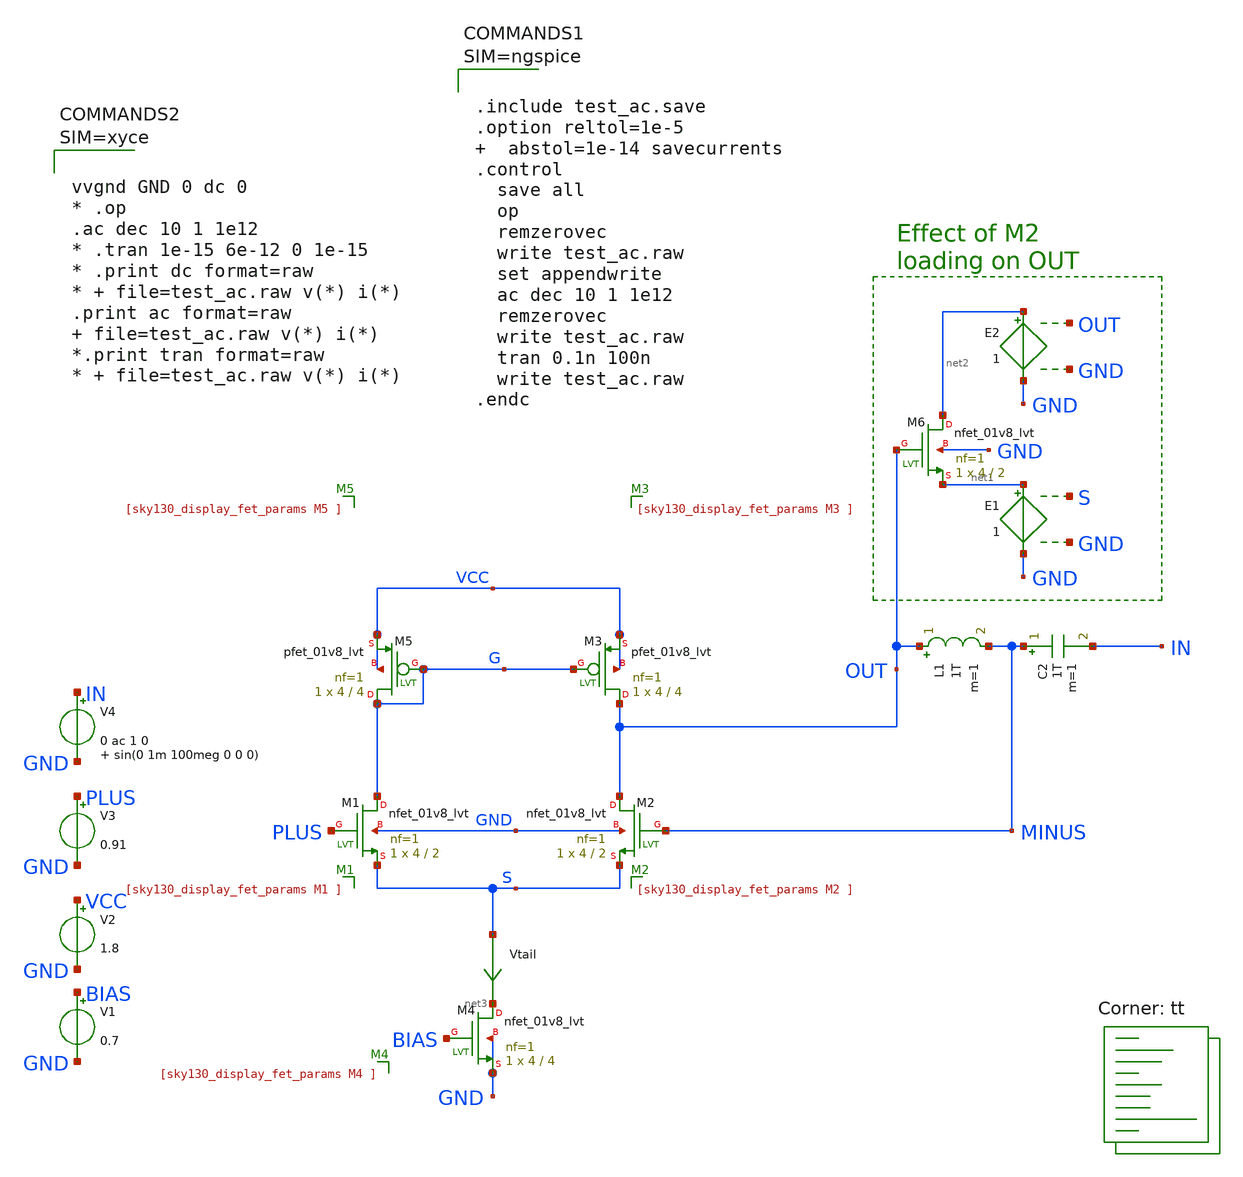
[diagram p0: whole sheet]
** sch_path: sky130A/xschem_libs/sky130_tests/test_ac/schematic/test_ac.sch
* Copyright 2021 Stefan Frederik Schippers
* Licensed under the Apache License, Version 2.0 (the "License");
* you may not use this file except in compliance with the License.
* You may obtain a copy of the License at
* https://www.apache.org/licenses/LICENSE-2.0
* Unless required by applicable law or agreed to in writing, software
* distributed under the License is distributed on an "AS IS" BASIS,
* WITHOUT WARRANTIES OR CONDITIONS OF ANY KIND, either express or implied.
* See the License for the specific language governing permissions and
* limitations under the License.
**.subckt test_ac
XM1 G PLUS S GND sky130_fd_pr__nfet_01v8_lvt L=2 W=4 nf=1 ad='int((1 + 1)/2) * 4 / 1 * 0.29' as='int((1 + 2)/2) * 4 / 1 * 0.29'
+ pd='2*int((1 + 1)/2) * (4 / 1 + 0.29)' ps='2*int((1 + 2)/2) * (4 / 1 + 0.29)' nrd='0.29 / 4 ' nrs='0.29 / 4 '
+ sa=0 sb=0 sd=0 mult=1 m=1
XM2 OUT MINUS S GND sky130_fd_pr__nfet_01v8_lvt L=2 W=4 nf=1 ad='int((1 + 1)/2) * 4 / 1 * 0.29' as='int((1 + 2)/2) * 4 / 1 * 0.29'
+ pd='2*int((1 + 1)/2) * (4 / 1 + 0.29)' ps='2*int((1 + 2)/2) * (4 / 1 + 0.29)' nrd='0.29 / 4 ' nrs='0.29 / 4 '
+ sa=0 sb=0 sd=0 mult=1 m=1
XM4 net3 BIAS GND GND sky130_fd_pr__nfet_01v8_lvt L=4 W=4 nf=1 ad='int((1 + 1)/2) * 4 / 1 * 0.29' as='int((1 + 2)/2) * 4 / 1 * 0.29'
+ pd='2*int((1 + 1)/2) * (4 / 1 + 0.29)' ps='2*int((1 + 2)/2) * (4 / 1 + 0.29)' nrd='0.29 / 4 ' nrs='0.29 / 4 '
+ sa=0 sb=0 sd=0 mult=1 m=1
XM3 OUT G VCC VCC sky130_fd_pr__pfet_01v8_lvt L=4 W=4 nf=1 ad='int((1 + 1)/2) * 4 / 1 * 0.29' as='int((1 + 2)/2) * 4 / 1 * 0.29'
+ pd='2*int((1 + 1)/2) * (4 / 1 + 0.29)' ps='2*int((1 + 2)/2) * (4 / 1 + 0.29)' nrd='0.29 / 4 ' nrs='0.29 / 4 '
+ sa=0 sb=0 sd=0 mult=1 m=1
XM5 G G VCC VCC sky130_fd_pr__pfet_01v8_lvt L=4 W=4 nf=1 ad='int((1 + 1)/2) * 4 / 1 * 0.29' as='int((1 + 2)/2) * 4 / 1 * 0.29'
+ pd='2*int((1 + 1)/2) * (4 / 1 + 0.29)' ps='2*int((1 + 2)/2) * (4 / 1 + 0.29)' nrd='0.29 / 4 ' nrs='0.29 / 4 '
+ sa=0 sb=0 sd=0 mult=1 m=1
Vtail S net3 0
.save i(vtail)
V1 BIAS GND 0.7
V2 VCC GND 1.8
V3 PLUS GND 0.91
V4 IN GND 0 ac 1 0 sin(0 1m 100meg 0 0 0)
C2 MINUS IN 1T m=1
L1 OUT MINUS 1T m=1
E1 net1 GND S GND 1
XM6 net2 OUT net1 GND sky130_fd_pr__nfet_01v8_lvt L=2 W=4 nf=1 ad='int((1 + 1)/2) * 4 / 1 * 0.29' as='int((1 + 2)/2) * 4 / 1 * 0.29'
+ pd='2*int((1 + 1)/2) * (4 / 1 + 0.29)' ps='2*int((1 + 2)/2) * (4 / 1 + 0.29)' nrd='0.29 / 4 ' nrs='0.29 / 4 '
+ sa=0 sb=0 sd=0 mult=1 m=1
E2 net2 GND OUT GND 1
**** begin user architecture code
.lib $::SKYWATER_MODELS/sky130.lib.spice tt



.include test_ac.save
.option reltol=1e-5   abstol=1e-14 savecurrents
.control
  save all
  op
  remzerovec
  write test_ac.raw
  set appendwrite
  ac dec 10 1 1e12
  remzerovec
  write test_ac.raw
  tran 0.1n 100n
  write test_ac.raw
.endc






**** end user architecture code
**.ends
.end
